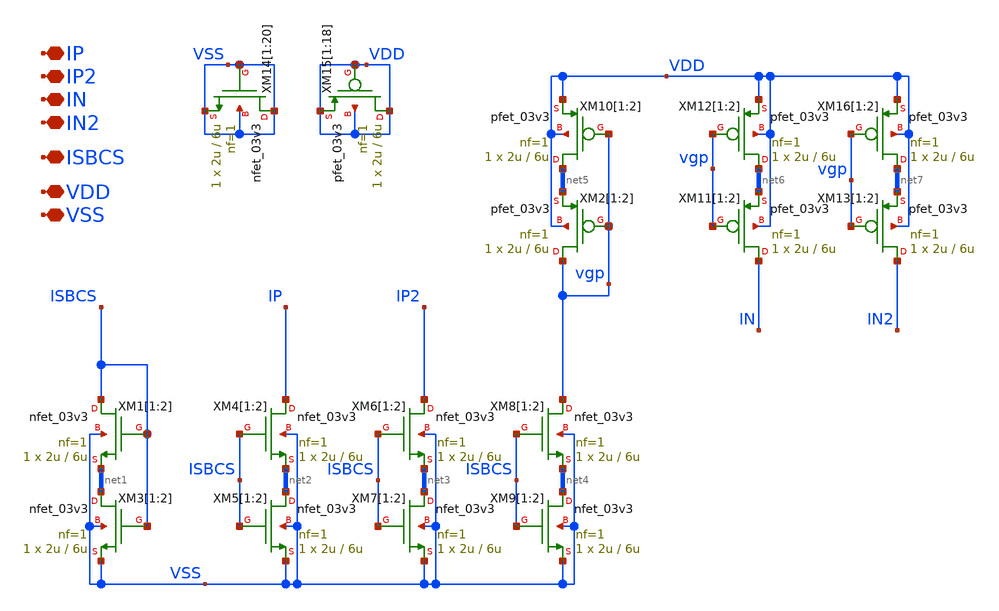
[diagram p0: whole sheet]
** sch_path: TIA_Filter/CurrentMirrors/CM_input.sch
**.subckt CM_input IP IP2 IN IN2 ISBCS VDD VSS
*.iopin IP
*.iopin IP2
*.iopin IN
*.iopin IN2
*.iopin ISBCS
*.iopin VDD
*.iopin VSS
XM1[1] ISBCS ISBCS net1[1] VSS nfet_03v3 L=6u W=2u nf=1 ad='int((nf+1)/2) * W/nf * 0.18u' as='int((nf+2)/2) * W/nf * 0.18u'
+ pd='2*int((nf+1)/2) * (W/nf + 0.18u)' ps='2*int((nf+2)/2) * (W/nf + 0.18u)' nrd='0.18u / W' nrs='0.18u / W'
+ sa=0 sb=0 sd=0 m=1
XM1[2] ISBCS ISBCS net1[0] VSS nfet_03v3 L=6u W=2u nf=1 ad='int((nf+1)/2) * W/nf * 0.18u' as='int((nf+2)/2) * W/nf * 0.18u'
+ pd='2*int((nf+1)/2) * (W/nf + 0.18u)' ps='2*int((nf+2)/2) * (W/nf + 0.18u)' nrd='0.18u / W' nrs='0.18u / W'
+ sa=0 sb=0 sd=0 m=1
XM2[1] vgp vgp net5[1] VDD pfet_03v3 L=6u W=2u nf=1 ad='int((nf+1)/2) * W/nf * 0.18u' as='int((nf+2)/2) * W/nf * 0.18u'
+ pd='2*int((nf+1)/2) * (W/nf + 0.18u)' ps='2*int((nf+2)/2) * (W/nf + 0.18u)' nrd='0.18u / W' nrs='0.18u / W'
+ sa=0 sb=0 sd=0 m=1
XM2[2] vgp vgp net5[0] VDD pfet_03v3 L=6u W=2u nf=1 ad='int((nf+1)/2) * W/nf * 0.18u' as='int((nf+2)/2) * W/nf * 0.18u'
+ pd='2*int((nf+1)/2) * (W/nf + 0.18u)' ps='2*int((nf+2)/2) * (W/nf + 0.18u)' nrd='0.18u / W' nrs='0.18u / W'
+ sa=0 sb=0 sd=0 m=1
XM3[1] net1[1] ISBCS VSS VSS nfet_03v3 L=6u W=2u nf=1 ad='int((nf+1)/2) * W/nf * 0.18u' as='int((nf+2)/2) * W/nf * 0.18u'
+ pd='2*int((nf+1)/2) * (W/nf + 0.18u)' ps='2*int((nf+2)/2) * (W/nf + 0.18u)' nrd='0.18u / W' nrs='0.18u / W'
+ sa=0 sb=0 sd=0 m=1
XM3[2] net1[0] ISBCS VSS VSS nfet_03v3 L=6u W=2u nf=1 ad='int((nf+1)/2) * W/nf * 0.18u' as='int((nf+2)/2) * W/nf * 0.18u'
+ pd='2*int((nf+1)/2) * (W/nf + 0.18u)' ps='2*int((nf+2)/2) * (W/nf + 0.18u)' nrd='0.18u / W' nrs='0.18u / W'
+ sa=0 sb=0 sd=0 m=1
XM4[1] IP ISBCS net2[1] VSS nfet_03v3 L=6u W=2u nf=1 ad='int((nf+1)/2) * W/nf * 0.18u' as='int((nf+2)/2) * W/nf * 0.18u'
+ pd='2*int((nf+1)/2) * (W/nf + 0.18u)' ps='2*int((nf+2)/2) * (W/nf + 0.18u)' nrd='0.18u / W' nrs='0.18u / W'
+ sa=0 sb=0 sd=0 m=1
XM4[2] IP ISBCS net2[0] VSS nfet_03v3 L=6u W=2u nf=1 ad='int((nf+1)/2) * W/nf * 0.18u' as='int((nf+2)/2) * W/nf * 0.18u'
+ pd='2*int((nf+1)/2) * (W/nf + 0.18u)' ps='2*int((nf+2)/2) * (W/nf + 0.18u)' nrd='0.18u / W' nrs='0.18u / W'
+ sa=0 sb=0 sd=0 m=1
XM5[1] net2[1] ISBCS VSS VSS nfet_03v3 L=6u W=2u nf=1 ad='int((nf+1)/2) * W/nf * 0.18u' as='int((nf+2)/2) * W/nf * 0.18u'
+ pd='2*int((nf+1)/2) * (W/nf + 0.18u)' ps='2*int((nf+2)/2) * (W/nf + 0.18u)' nrd='0.18u / W' nrs='0.18u / W'
+ sa=0 sb=0 sd=0 m=1
XM5[2] net2[0] ISBCS VSS VSS nfet_03v3 L=6u W=2u nf=1 ad='int((nf+1)/2) * W/nf * 0.18u' as='int((nf+2)/2) * W/nf * 0.18u'
+ pd='2*int((nf+1)/2) * (W/nf + 0.18u)' ps='2*int((nf+2)/2) * (W/nf + 0.18u)' nrd='0.18u / W' nrs='0.18u / W'
+ sa=0 sb=0 sd=0 m=1
XM6[1] IP2 ISBCS net3[1] VSS nfet_03v3 L=6u W=2u nf=1 ad='int((nf+1)/2) * W/nf * 0.18u' as='int((nf+2)/2) * W/nf * 0.18u'
+ pd='2*int((nf+1)/2) * (W/nf + 0.18u)' ps='2*int((nf+2)/2) * (W/nf + 0.18u)' nrd='0.18u / W' nrs='0.18u / W'
+ sa=0 sb=0 sd=0 m=1
XM6[2] IP2 ISBCS net3[0] VSS nfet_03v3 L=6u W=2u nf=1 ad='int((nf+1)/2) * W/nf * 0.18u' as='int((nf+2)/2) * W/nf * 0.18u'
+ pd='2*int((nf+1)/2) * (W/nf + 0.18u)' ps='2*int((nf+2)/2) * (W/nf + 0.18u)' nrd='0.18u / W' nrs='0.18u / W'
+ sa=0 sb=0 sd=0 m=1
XM7[1] net3[1] ISBCS VSS VSS nfet_03v3 L=6u W=2u nf=1 ad='int((nf+1)/2) * W/nf * 0.18u' as='int((nf+2)/2) * W/nf * 0.18u'
+ pd='2*int((nf+1)/2) * (W/nf + 0.18u)' ps='2*int((nf+2)/2) * (W/nf + 0.18u)' nrd='0.18u / W' nrs='0.18u / W'
+ sa=0 sb=0 sd=0 m=1
XM7[2] net3[0] ISBCS VSS VSS nfet_03v3 L=6u W=2u nf=1 ad='int((nf+1)/2) * W/nf * 0.18u' as='int((nf+2)/2) * W/nf * 0.18u'
+ pd='2*int((nf+1)/2) * (W/nf + 0.18u)' ps='2*int((nf+2)/2) * (W/nf + 0.18u)' nrd='0.18u / W' nrs='0.18u / W'
+ sa=0 sb=0 sd=0 m=1
XM8[1] vgp ISBCS net4[1] VSS nfet_03v3 L=6u W=2u nf=1 ad='int((nf+1)/2) * W/nf * 0.18u' as='int((nf+2)/2) * W/nf * 0.18u'
+ pd='2*int((nf+1)/2) * (W/nf + 0.18u)' ps='2*int((nf+2)/2) * (W/nf + 0.18u)' nrd='0.18u / W' nrs='0.18u / W'
+ sa=0 sb=0 sd=0 m=1
XM8[2] vgp ISBCS net4[0] VSS nfet_03v3 L=6u W=2u nf=1 ad='int((nf+1)/2) * W/nf * 0.18u' as='int((nf+2)/2) * W/nf * 0.18u'
+ pd='2*int((nf+1)/2) * (W/nf + 0.18u)' ps='2*int((nf+2)/2) * (W/nf + 0.18u)' nrd='0.18u / W' nrs='0.18u / W'
+ sa=0 sb=0 sd=0 m=1
XM9[1] net4[1] ISBCS VSS VSS nfet_03v3 L=6u W=2u nf=1 ad='int((nf+1)/2) * W/nf * 0.18u' as='int((nf+2)/2) * W/nf * 0.18u'
+ pd='2*int((nf+1)/2) * (W/nf + 0.18u)' ps='2*int((nf+2)/2) * (W/nf + 0.18u)' nrd='0.18u / W' nrs='0.18u / W'
+ sa=0 sb=0 sd=0 m=1
XM9[2] net4[0] ISBCS VSS VSS nfet_03v3 L=6u W=2u nf=1 ad='int((nf+1)/2) * W/nf * 0.18u' as='int((nf+2)/2) * W/nf * 0.18u'
+ pd='2*int((nf+1)/2) * (W/nf + 0.18u)' ps='2*int((nf+2)/2) * (W/nf + 0.18u)' nrd='0.18u / W' nrs='0.18u / W'
+ sa=0 sb=0 sd=0 m=1
XM10[1] net5[1] vgp VDD VDD pfet_03v3 L=6u W=2u nf=1 ad='int((nf+1)/2) * W/nf * 0.18u' as='int((nf+2)/2) * W/nf * 0.18u'
+ pd='2*int((nf+1)/2) * (W/nf + 0.18u)' ps='2*int((nf+2)/2) * (W/nf + 0.18u)' nrd='0.18u / W' nrs='0.18u / W'
+ sa=0 sb=0 sd=0 m=1
XM10[2] net5[0] vgp VDD VDD pfet_03v3 L=6u W=2u nf=1 ad='int((nf+1)/2) * W/nf * 0.18u' as='int((nf+2)/2) * W/nf * 0.18u'
+ pd='2*int((nf+1)/2) * (W/nf + 0.18u)' ps='2*int((nf+2)/2) * (W/nf + 0.18u)' nrd='0.18u / W' nrs='0.18u / W'
+ sa=0 sb=0 sd=0 m=1
XM11[1] IN vgp net6[1] VDD pfet_03v3 L=6u W=2u nf=1 ad='int((nf+1)/2) * W/nf * 0.18u' as='int((nf+2)/2) * W/nf * 0.18u'
+ pd='2*int((nf+1)/2) * (W/nf + 0.18u)' ps='2*int((nf+2)/2) * (W/nf + 0.18u)' nrd='0.18u / W' nrs='0.18u / W'
+ sa=0 sb=0 sd=0 m=1
XM11[2] IN vgp net6[0] VDD pfet_03v3 L=6u W=2u nf=1 ad='int((nf+1)/2) * W/nf * 0.18u' as='int((nf+2)/2) * W/nf * 0.18u'
+ pd='2*int((nf+1)/2) * (W/nf + 0.18u)' ps='2*int((nf+2)/2) * (W/nf + 0.18u)' nrd='0.18u / W' nrs='0.18u / W'
+ sa=0 sb=0 sd=0 m=1
XM12[1] net6[1] vgp VDD VDD pfet_03v3 L=6u W=2u nf=1 ad='int((nf+1)/2) * W/nf * 0.18u' as='int((nf+2)/2) * W/nf * 0.18u'
+ pd='2*int((nf+1)/2) * (W/nf + 0.18u)' ps='2*int((nf+2)/2) * (W/nf + 0.18u)' nrd='0.18u / W' nrs='0.18u / W'
+ sa=0 sb=0 sd=0 m=1
XM12[2] net6[0] vgp VDD VDD pfet_03v3 L=6u W=2u nf=1 ad='int((nf+1)/2) * W/nf * 0.18u' as='int((nf+2)/2) * W/nf * 0.18u'
+ pd='2*int((nf+1)/2) * (W/nf + 0.18u)' ps='2*int((nf+2)/2) * (W/nf + 0.18u)' nrd='0.18u / W' nrs='0.18u / W'
+ sa=0 sb=0 sd=0 m=1
XM13[1] IN2 vgp net7[1] VDD pfet_03v3 L=6u W=2u nf=1 ad='int((nf+1)/2) * W/nf * 0.18u' as='int((nf+2)/2) * W/nf * 0.18u'
+ pd='2*int((nf+1)/2) * (W/nf + 0.18u)' ps='2*int((nf+2)/2) * (W/nf + 0.18u)' nrd='0.18u / W' nrs='0.18u / W'
+ sa=0 sb=0 sd=0 m=1
XM13[2] IN2 vgp net7[0] VDD pfet_03v3 L=6u W=2u nf=1 ad='int((nf+1)/2) * W/nf * 0.18u' as='int((nf+2)/2) * W/nf * 0.18u'
+ pd='2*int((nf+1)/2) * (W/nf + 0.18u)' ps='2*int((nf+2)/2) * (W/nf + 0.18u)' nrd='0.18u / W' nrs='0.18u / W'
+ sa=0 sb=0 sd=0 m=1
XM16[1] net7[1] vgp VDD VDD pfet_03v3 L=6u W=2u nf=1 ad='int((nf+1)/2) * W/nf * 0.18u' as='int((nf+2)/2) * W/nf * 0.18u'
+ pd='2*int((nf+1)/2) * (W/nf + 0.18u)' ps='2*int((nf+2)/2) * (W/nf + 0.18u)' nrd='0.18u / W' nrs='0.18u / W'
+ sa=0 sb=0 sd=0 m=1
XM16[2] net7[0] vgp VDD VDD pfet_03v3 L=6u W=2u nf=1 ad='int((nf+1)/2) * W/nf * 0.18u' as='int((nf+2)/2) * W/nf * 0.18u'
+ pd='2*int((nf+1)/2) * (W/nf + 0.18u)' ps='2*int((nf+2)/2) * (W/nf + 0.18u)' nrd='0.18u / W' nrs='0.18u / W'
+ sa=0 sb=0 sd=0 m=1
XM14[1] VSS VSS VSS VSS nfet_03v3 L=6u W=2u nf=1 ad='int((nf+1)/2) * W/nf * 0.18u' as='int((nf+2)/2) * W/nf * 0.18u'
+ pd='2*int((nf+1)/2) * (W/nf + 0.18u)' ps='2*int((nf+2)/2) * (W/nf + 0.18u)' nrd='0.18u / W' nrs='0.18u / W'
+ sa=0 sb=0 sd=0 m=1
XM14[2] VSS VSS VSS VSS nfet_03v3 L=6u W=2u nf=1 ad='int((nf+1)/2) * W/nf * 0.18u' as='int((nf+2)/2) * W/nf * 0.18u'
+ pd='2*int((nf+1)/2) * (W/nf + 0.18u)' ps='2*int((nf+2)/2) * (W/nf + 0.18u)' nrd='0.18u / W' nrs='0.18u / W'
+ sa=0 sb=0 sd=0 m=1
XM14[3] VSS VSS VSS VSS nfet_03v3 L=6u W=2u nf=1 ad='int((nf+1)/2) * W/nf * 0.18u' as='int((nf+2)/2) * W/nf * 0.18u'
+ pd='2*int((nf+1)/2) * (W/nf + 0.18u)' ps='2*int((nf+2)/2) * (W/nf + 0.18u)' nrd='0.18u / W' nrs='0.18u / W'
+ sa=0 sb=0 sd=0 m=1
XM14[4] VSS VSS VSS VSS nfet_03v3 L=6u W=2u nf=1 ad='int((nf+1)/2) * W/nf * 0.18u' as='int((nf+2)/2) * W/nf * 0.18u'
+ pd='2*int((nf+1)/2) * (W/nf + 0.18u)' ps='2*int((nf+2)/2) * (W/nf + 0.18u)' nrd='0.18u / W' nrs='0.18u / W'
+ sa=0 sb=0 sd=0 m=1
XM14[5] VSS VSS VSS VSS nfet_03v3 L=6u W=2u nf=1 ad='int((nf+1)/2) * W/nf * 0.18u' as='int((nf+2)/2) * W/nf * 0.18u'
+ pd='2*int((nf+1)/2) * (W/nf + 0.18u)' ps='2*int((nf+2)/2) * (W/nf + 0.18u)' nrd='0.18u / W' nrs='0.18u / W'
+ sa=0 sb=0 sd=0 m=1
XM14[6] VSS VSS VSS VSS nfet_03v3 L=6u W=2u nf=1 ad='int((nf+1)/2) * W/nf * 0.18u' as='int((nf+2)/2) * W/nf * 0.18u'
+ pd='2*int((nf+1)/2) * (W/nf + 0.18u)' ps='2*int((nf+2)/2) * (W/nf + 0.18u)' nrd='0.18u / W' nrs='0.18u / W'
+ sa=0 sb=0 sd=0 m=1
XM14[7] VSS VSS VSS VSS nfet_03v3 L=6u W=2u nf=1 ad='int((nf+1)/2) * W/nf * 0.18u' as='int((nf+2)/2) * W/nf * 0.18u'
+ pd='2*int((nf+1)/2) * (W/nf + 0.18u)' ps='2*int((nf+2)/2) * (W/nf + 0.18u)' nrd='0.18u / W' nrs='0.18u / W'
+ sa=0 sb=0 sd=0 m=1
XM14[8] VSS VSS VSS VSS nfet_03v3 L=6u W=2u nf=1 ad='int((nf+1)/2) * W/nf * 0.18u' as='int((nf+2)/2) * W/nf * 0.18u'
+ pd='2*int((nf+1)/2) * (W/nf + 0.18u)' ps='2*int((nf+2)/2) * (W/nf + 0.18u)' nrd='0.18u / W' nrs='0.18u / W'
+ sa=0 sb=0 sd=0 m=1
XM14[9] VSS VSS VSS VSS nfet_03v3 L=6u W=2u nf=1 ad='int((nf+1)/2) * W/nf * 0.18u' as='int((nf+2)/2) * W/nf * 0.18u'
+ pd='2*int((nf+1)/2) * (W/nf + 0.18u)' ps='2*int((nf+2)/2) * (W/nf + 0.18u)' nrd='0.18u / W' nrs='0.18u / W'
+ sa=0 sb=0 sd=0 m=1
XM14[10] VSS VSS VSS VSS nfet_03v3 L=6u W=2u nf=1 ad='int((nf+1)/2) * W/nf * 0.18u' as='int((nf+2)/2) * W/nf * 0.18u'
+ pd='2*int((nf+1)/2) * (W/nf + 0.18u)' ps='2*int((nf+2)/2) * (W/nf + 0.18u)' nrd='0.18u / W' nrs='0.18u / W'
+ sa=0 sb=0 sd=0 m=1
XM14[11] VSS VSS VSS VSS nfet_03v3 L=6u W=2u nf=1 ad='int((nf+1)/2) * W/nf * 0.18u' as='int((nf+2)/2) * W/nf * 0.18u'
+ pd='2*int((nf+1)/2) * (W/nf + 0.18u)' ps='2*int((nf+2)/2) * (W/nf + 0.18u)' nrd='0.18u / W' nrs='0.18u / W'
+ sa=0 sb=0 sd=0 m=1
XM14[12] VSS VSS VSS VSS nfet_03v3 L=6u W=2u nf=1 ad='int((nf+1)/2) * W/nf * 0.18u' as='int((nf+2)/2) * W/nf * 0.18u'
+ pd='2*int((nf+1)/2) * (W/nf + 0.18u)' ps='2*int((nf+2)/2) * (W/nf + 0.18u)' nrd='0.18u / W' nrs='0.18u / W'
+ sa=0 sb=0 sd=0 m=1
XM14[13] VSS VSS VSS VSS nfet_03v3 L=6u W=2u nf=1 ad='int((nf+1)/2) * W/nf * 0.18u' as='int((nf+2)/2) * W/nf * 0.18u'
+ pd='2*int((nf+1)/2) * (W/nf + 0.18u)' ps='2*int((nf+2)/2) * (W/nf + 0.18u)' nrd='0.18u / W' nrs='0.18u / W'
+ sa=0 sb=0 sd=0 m=1
XM14[14] VSS VSS VSS VSS nfet_03v3 L=6u W=2u nf=1 ad='int((nf+1)/2) * W/nf * 0.18u' as='int((nf+2)/2) * W/nf * 0.18u'
+ pd='2*int((nf+1)/2) * (W/nf + 0.18u)' ps='2*int((nf+2)/2) * (W/nf + 0.18u)' nrd='0.18u / W' nrs='0.18u / W'
+ sa=0 sb=0 sd=0 m=1
XM14[15] VSS VSS VSS VSS nfet_03v3 L=6u W=2u nf=1 ad='int((nf+1)/2) * W/nf * 0.18u' as='int((nf+2)/2) * W/nf * 0.18u'
+ pd='2*int((nf+1)/2) * (W/nf + 0.18u)' ps='2*int((nf+2)/2) * (W/nf + 0.18u)' nrd='0.18u / W' nrs='0.18u / W'
+ sa=0 sb=0 sd=0 m=1
XM14[16] VSS VSS VSS VSS nfet_03v3 L=6u W=2u nf=1 ad='int((nf+1)/2) * W/nf * 0.18u' as='int((nf+2)/2) * W/nf * 0.18u'
+ pd='2*int((nf+1)/2) * (W/nf + 0.18u)' ps='2*int((nf+2)/2) * (W/nf + 0.18u)' nrd='0.18u / W' nrs='0.18u / W'
+ sa=0 sb=0 sd=0 m=1
XM14[17] VSS VSS VSS VSS nfet_03v3 L=6u W=2u nf=1 ad='int((nf+1)/2) * W/nf * 0.18u' as='int((nf+2)/2) * W/nf * 0.18u'
+ pd='2*int((nf+1)/2) * (W/nf + 0.18u)' ps='2*int((nf+2)/2) * (W/nf + 0.18u)' nrd='0.18u / W' nrs='0.18u / W'
+ sa=0 sb=0 sd=0 m=1
XM14[18] VSS VSS VSS VSS nfet_03v3 L=6u W=2u nf=1 ad='int((nf+1)/2) * W/nf * 0.18u' as='int((nf+2)/2) * W/nf * 0.18u'
+ pd='2*int((nf+1)/2) * (W/nf + 0.18u)' ps='2*int((nf+2)/2) * (W/nf + 0.18u)' nrd='0.18u / W' nrs='0.18u / W'
+ sa=0 sb=0 sd=0 m=1
XM14[19] VSS VSS VSS VSS nfet_03v3 L=6u W=2u nf=1 ad='int((nf+1)/2) * W/nf * 0.18u' as='int((nf+2)/2) * W/nf * 0.18u'
+ pd='2*int((nf+1)/2) * (W/nf + 0.18u)' ps='2*int((nf+2)/2) * (W/nf + 0.18u)' nrd='0.18u / W' nrs='0.18u / W'
+ sa=0 sb=0 sd=0 m=1
XM14[20] VSS VSS VSS VSS nfet_03v3 L=6u W=2u nf=1 ad='int((nf+1)/2) * W/nf * 0.18u' as='int((nf+2)/2) * W/nf * 0.18u'
+ pd='2*int((nf+1)/2) * (W/nf + 0.18u)' ps='2*int((nf+2)/2) * (W/nf + 0.18u)' nrd='0.18u / W' nrs='0.18u / W'
+ sa=0 sb=0 sd=0 m=1
XM15[1] VDD VDD VDD VDD pfet_03v3 L=6u W=2u nf=1 ad='int((nf+1)/2) * W/nf * 0.18u' as='int((nf+2)/2) * W/nf * 0.18u'
+ pd='2*int((nf+1)/2) * (W/nf + 0.18u)' ps='2*int((nf+2)/2) * (W/nf + 0.18u)' nrd='0.18u / W' nrs='0.18u / W'
+ sa=0 sb=0 sd=0 m=1
XM15[2] VDD VDD VDD VDD pfet_03v3 L=6u W=2u nf=1 ad='int((nf+1)/2) * W/nf * 0.18u' as='int((nf+2)/2) * W/nf * 0.18u'
+ pd='2*int((nf+1)/2) * (W/nf + 0.18u)' ps='2*int((nf+2)/2) * (W/nf + 0.18u)' nrd='0.18u / W' nrs='0.18u / W'
+ sa=0 sb=0 sd=0 m=1
XM15[3] VDD VDD VDD VDD pfet_03v3 L=6u W=2u nf=1 ad='int((nf+1)/2) * W/nf * 0.18u' as='int((nf+2)/2) * W/nf * 0.18u'
+ pd='2*int((nf+1)/2) * (W/nf + 0.18u)' ps='2*int((nf+2)/2) * (W/nf + 0.18u)' nrd='0.18u / W' nrs='0.18u / W'
+ sa=0 sb=0 sd=0 m=1
XM15[4] VDD VDD VDD VDD pfet_03v3 L=6u W=2u nf=1 ad='int((nf+1)/2) * W/nf * 0.18u' as='int((nf+2)/2) * W/nf * 0.18u'
+ pd='2*int((nf+1)/2) * (W/nf + 0.18u)' ps='2*int((nf+2)/2) * (W/nf + 0.18u)' nrd='0.18u / W' nrs='0.18u / W'
+ sa=0 sb=0 sd=0 m=1
XM15[5] VDD VDD VDD VDD pfet_03v3 L=6u W=2u nf=1 ad='int((nf+1)/2) * W/nf * 0.18u' as='int((nf+2)/2) * W/nf * 0.18u'
+ pd='2*int((nf+1)/2) * (W/nf + 0.18u)' ps='2*int((nf+2)/2) * (W/nf + 0.18u)' nrd='0.18u / W' nrs='0.18u / W'
+ sa=0 sb=0 sd=0 m=1
XM15[6] VDD VDD VDD VDD pfet_03v3 L=6u W=2u nf=1 ad='int((nf+1)/2) * W/nf * 0.18u' as='int((nf+2)/2) * W/nf * 0.18u'
+ pd='2*int((nf+1)/2) * (W/nf + 0.18u)' ps='2*int((nf+2)/2) * (W/nf + 0.18u)' nrd='0.18u / W' nrs='0.18u / W'
+ sa=0 sb=0 sd=0 m=1
XM15[7] VDD VDD VDD VDD pfet_03v3 L=6u W=2u nf=1 ad='int((nf+1)/2) * W/nf * 0.18u' as='int((nf+2)/2) * W/nf * 0.18u'
+ pd='2*int((nf+1)/2) * (W/nf + 0.18u)' ps='2*int((nf+2)/2) * (W/nf + 0.18u)' nrd='0.18u / W' nrs='0.18u / W'
+ sa=0 sb=0 sd=0 m=1
XM15[8] VDD VDD VDD VDD pfet_03v3 L=6u W=2u nf=1 ad='int((nf+1)/2) * W/nf * 0.18u' as='int((nf+2)/2) * W/nf * 0.18u'
+ pd='2*int((nf+1)/2) * (W/nf + 0.18u)' ps='2*int((nf+2)/2) * (W/nf + 0.18u)' nrd='0.18u / W' nrs='0.18u / W'
+ sa=0 sb=0 sd=0 m=1
XM15[9] VDD VDD VDD VDD pfet_03v3 L=6u W=2u nf=1 ad='int((nf+1)/2) * W/nf * 0.18u' as='int((nf+2)/2) * W/nf * 0.18u'
+ pd='2*int((nf+1)/2) * (W/nf + 0.18u)' ps='2*int((nf+2)/2) * (W/nf + 0.18u)' nrd='0.18u / W' nrs='0.18u / W'
+ sa=0 sb=0 sd=0 m=1
XM15[10] VDD VDD VDD VDD pfet_03v3 L=6u W=2u nf=1 ad='int((nf+1)/2) * W/nf * 0.18u' as='int((nf+2)/2) * W/nf * 0.18u'
+ pd='2*int((nf+1)/2) * (W/nf + 0.18u)' ps='2*int((nf+2)/2) * (W/nf + 0.18u)' nrd='0.18u / W' nrs='0.18u / W'
+ sa=0 sb=0 sd=0 m=1
XM15[11] VDD VDD VDD VDD pfet_03v3 L=6u W=2u nf=1 ad='int((nf+1)/2) * W/nf * 0.18u' as='int((nf+2)/2) * W/nf * 0.18u'
+ pd='2*int((nf+1)/2) * (W/nf + 0.18u)' ps='2*int((nf+2)/2) * (W/nf + 0.18u)' nrd='0.18u / W' nrs='0.18u / W'
+ sa=0 sb=0 sd=0 m=1
XM15[12] VDD VDD VDD VDD pfet_03v3 L=6u W=2u nf=1 ad='int((nf+1)/2) * W/nf * 0.18u' as='int((nf+2)/2) * W/nf * 0.18u'
+ pd='2*int((nf+1)/2) * (W/nf + 0.18u)' ps='2*int((nf+2)/2) * (W/nf + 0.18u)' nrd='0.18u / W' nrs='0.18u / W'
+ sa=0 sb=0 sd=0 m=1
XM15[13] VDD VDD VDD VDD pfet_03v3 L=6u W=2u nf=1 ad='int((nf+1)/2) * W/nf * 0.18u' as='int((nf+2)/2) * W/nf * 0.18u'
+ pd='2*int((nf+1)/2) * (W/nf + 0.18u)' ps='2*int((nf+2)/2) * (W/nf + 0.18u)' nrd='0.18u / W' nrs='0.18u / W'
+ sa=0 sb=0 sd=0 m=1
XM15[14] VDD VDD VDD VDD pfet_03v3 L=6u W=2u nf=1 ad='int((nf+1)/2) * W/nf * 0.18u' as='int((nf+2)/2) * W/nf * 0.18u'
+ pd='2*int((nf+1)/2) * (W/nf + 0.18u)' ps='2*int((nf+2)/2) * (W/nf + 0.18u)' nrd='0.18u / W' nrs='0.18u / W'
+ sa=0 sb=0 sd=0 m=1
XM15[15] VDD VDD VDD VDD pfet_03v3 L=6u W=2u nf=1 ad='int((nf+1)/2) * W/nf * 0.18u' as='int((nf+2)/2) * W/nf * 0.18u'
+ pd='2*int((nf+1)/2) * (W/nf + 0.18u)' ps='2*int((nf+2)/2) * (W/nf + 0.18u)' nrd='0.18u / W' nrs='0.18u / W'
+ sa=0 sb=0 sd=0 m=1
XM15[16] VDD VDD VDD VDD pfet_03v3 L=6u W=2u nf=1 ad='int((nf+1)/2) * W/nf * 0.18u' as='int((nf+2)/2) * W/nf * 0.18u'
+ pd='2*int((nf+1)/2) * (W/nf + 0.18u)' ps='2*int((nf+2)/2) * (W/nf + 0.18u)' nrd='0.18u / W' nrs='0.18u / W'
+ sa=0 sb=0 sd=0 m=1
XM15[17] VDD VDD VDD VDD pfet_03v3 L=6u W=2u nf=1 ad='int((nf+1)/2) * W/nf * 0.18u' as='int((nf+2)/2) * W/nf * 0.18u'
+ pd='2*int((nf+1)/2) * (W/nf + 0.18u)' ps='2*int((nf+2)/2) * (W/nf + 0.18u)' nrd='0.18u / W' nrs='0.18u / W'
+ sa=0 sb=0 sd=0 m=1
XM15[18] VDD VDD VDD VDD pfet_03v3 L=6u W=2u nf=1 ad='int((nf+1)/2) * W/nf * 0.18u' as='int((nf+2)/2) * W/nf * 0.18u'
+ pd='2*int((nf+1)/2) * (W/nf + 0.18u)' ps='2*int((nf+2)/2) * (W/nf + 0.18u)' nrd='0.18u / W' nrs='0.18u / W'
+ sa=0 sb=0 sd=0 m=1
**.ends
.end
